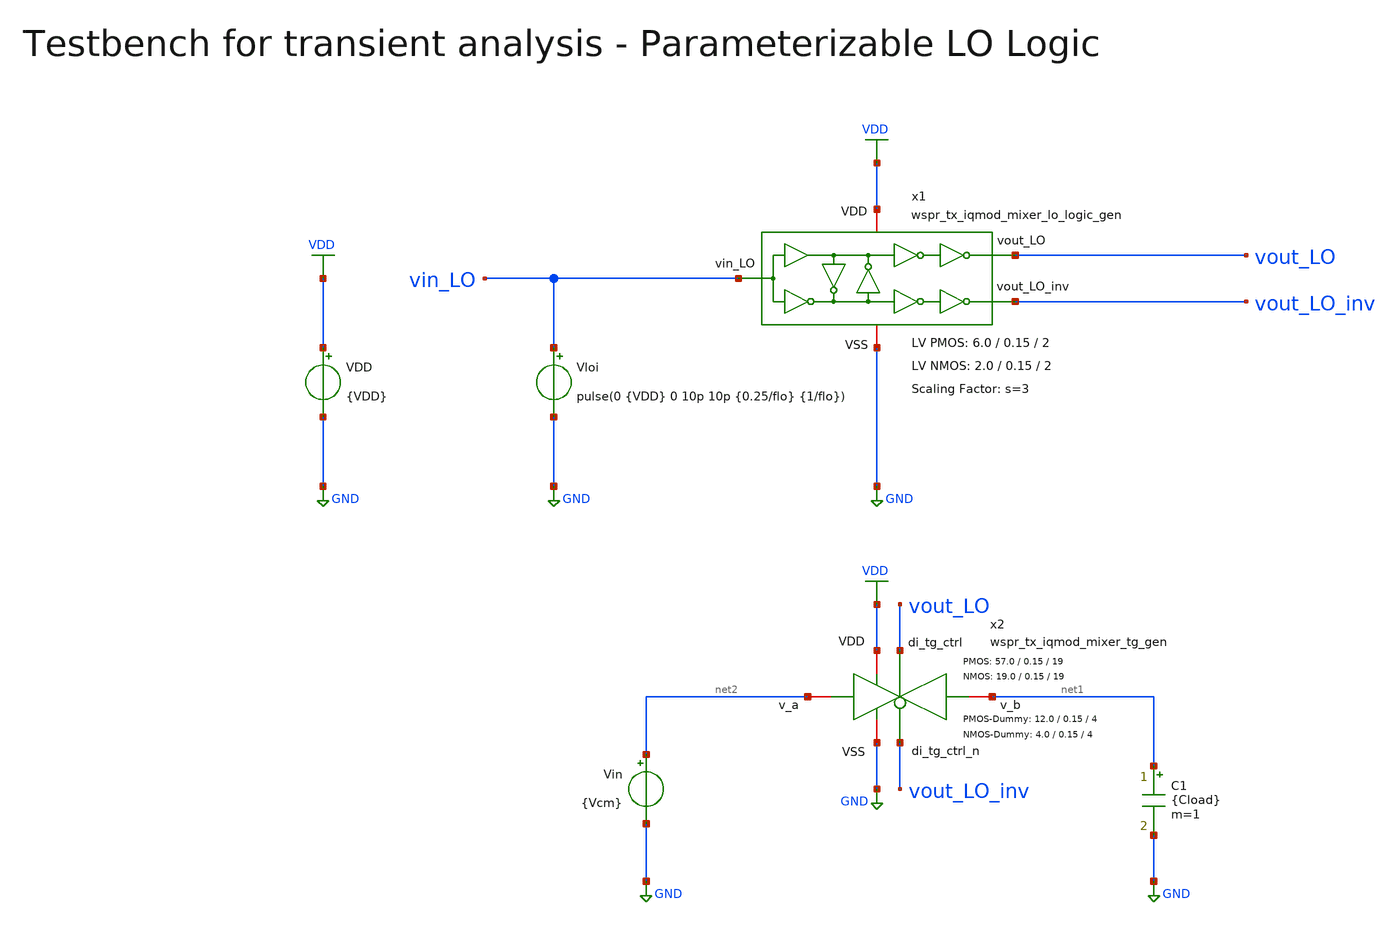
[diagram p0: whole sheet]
** sch_path: sky130/macros/iqmod/testbenches/wspr_tx_iqmod_mixer_lo_logic_tb_tran.sch
**.subckt wspr_tx_iqmod_mixer_lo_logic_tb_tran
VDD VDD GND {VDD}
C1 net1 GND {Cload} m=1
x1 VDD vin_LO vout_LO GND vout_LO_inv wspr_tx_iqmod_mixer_lo_logic_gen W_P=6.0 L_P=0.15 NF_P=2
+ W_N=2.0 L_N=0.15 NF_N=2 s=3
Vloi vin_LO GND pulse(0 {VDD} 0 10p 10p {0.25/flo} {1/flo})
Vin net2 GND {Vcm}
x2 VDD vout_LO GND net1 net2 vout_LO_inv wspr_tx_iqmod_mixer_tg_gen W_P=57.0 L_P=0.15 NF_P=19
+ W_N=19.0 L_N=0.15 NF_N=19 W_P_D=12.0 L_P_D=0.15 NF_P_D=4 W_N_D=4.0 L_N_D=0.15 NF_N_D=4
**** begin user architecture code


.param VDD=1.8
.param Vcm=VDD/2
.param temp=27
.param flo=10e6
.csparam flo=flo
.param Cload=1p
.options savecurrents klu method=gear reltol=1e-4 abstol=1e-15 gmin=1e-15
.control
save all

* User Constants
let tstop = 2*1/flo
let tstep = 0.01*1/flo

* Operating Point Analysis
op
remzerovec
write wspr_tx_iqmod_mixer_lo_logic_tb_tran.raw
set appendwrite

* Transient Analysis
tran $&tstep $&tstop
write wspr_tx_iqmod_mixer_lo_logic_tb_tran.raw

quit
.endc


.lib $::SKYWATER_MODELS/sky130.lib.spice tt
**** end user architecture code
**.ends
.GLOBAL GND
.GLOBAL VDD
.end
